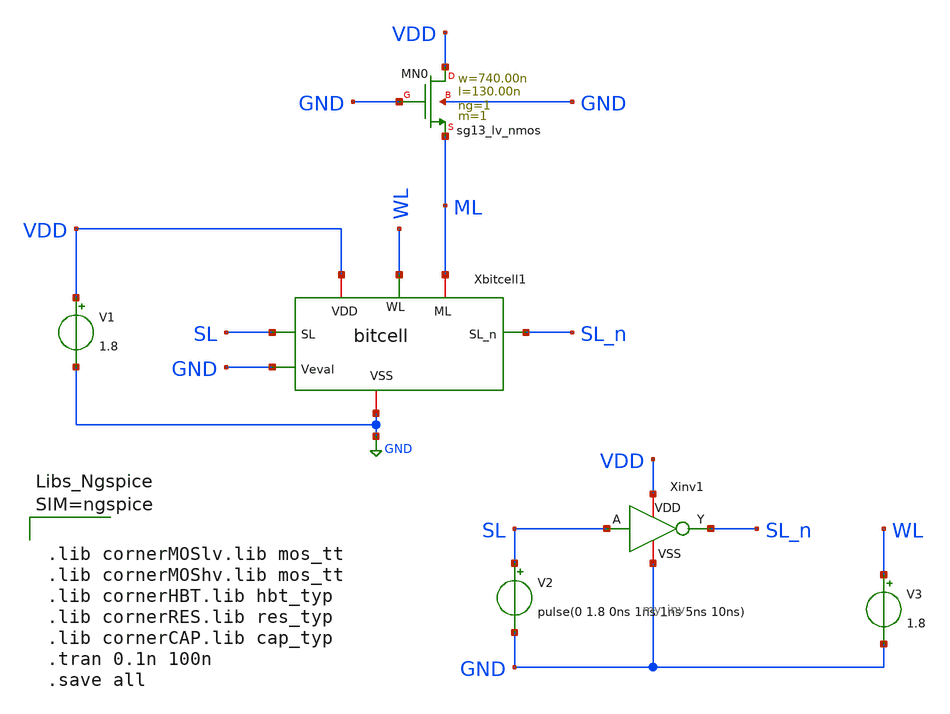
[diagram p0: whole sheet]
** sch_path: xschem/bitcell_TB.sch
**.subckt bitcell_TB
Xbitcell1 WL SL SL_n VDD ML GND GND bitcell
V1 VDD GND 1.8
V2 SL GND pulse(0 1.8 0ns 1ns 1ns 5ns 10ns)
Xinv1 VDD SL_n SL GND my_inv
V3 WL GND 1.8
XMN0 VDD GND ML GND sg13_lv_nmos w=740.00n l=130.00n ng=1 m=1 mm_ok=1
**** begin user architecture code



.lib cornerMOSlv.lib mos_tt
.lib cornerMOShv.lib mos_tt
.lib cornerHBT.lib hbt_typ
.lib cornerRES.lib res_typ
.lib cornerCAP.lib cap_typ
.tran 0.1n 100n
.save all



**** end user architecture code
**.ends

* expanding   symbol:  bitcell.sym # of pins=7
** sym_path: xschem/bitcell.sym
** sch_path: xschem/bitcell.sch
.subckt bitcell WL SL SL_n VDD ML Veval VSS
*.ipin SL
*.ipin SL_n
*.ipin WL
*.iopin ML
*.ipin Veval
*.iopin VDD
*.iopin VSS
XMN1 SL WL D_n VSS sg13_lv_nmos w=740.00n l=130.00n ng=1 m=1 mm_ok=1
XMN2 SL_n WL D VSS sg13_lv_nmos w=740.00n l=130.00n ng=1 m=1 mm_ok=1
XMN3 net1 D_n SL VSS sg13_lv_nmos w=740.00n l=130.00n ng=1 m=1 mm_ok=1
XMN4 net1 D SL_n VSS sg13_lv_nmos w=740.00n l=130.00n ng=1 m=1 mm_ok=1
XMN5 ML net1 net2 VSS sg13_lv_nmos w=740.00n l=130.00n ng=1 m=1 mm_ok=1
XMN6 net2 Veval VSS VSS sg13_lv_nmos w=740.00n l=130.00n ng=1 m=1 mm_ok=1
X1 VDD D D_n VSS my_inv
X2 VDD D_n D VSS my_inv
.ends


* expanding   symbol:  my_inv.sym # of pins=4
** sym_path: xschem/my_inv.sym
** sch_path: xschem/my_inv.sch
.subckt my_inv VDD Y A VSS
*.opin Y
*.ipin A
*.iopin VDD
*.iopin VSS
XMN0 Y A VSS VSS sg13_lv_nmos w=740.00n l=130.00n ng=1 m=1 mm_ok=1
XMP0 Y A VDD VDD sg13_lv_pmos w=1.12u l=130.00n ng=1 m=1 mm_ok=1
.ends

.GLOBAL GND
.end
